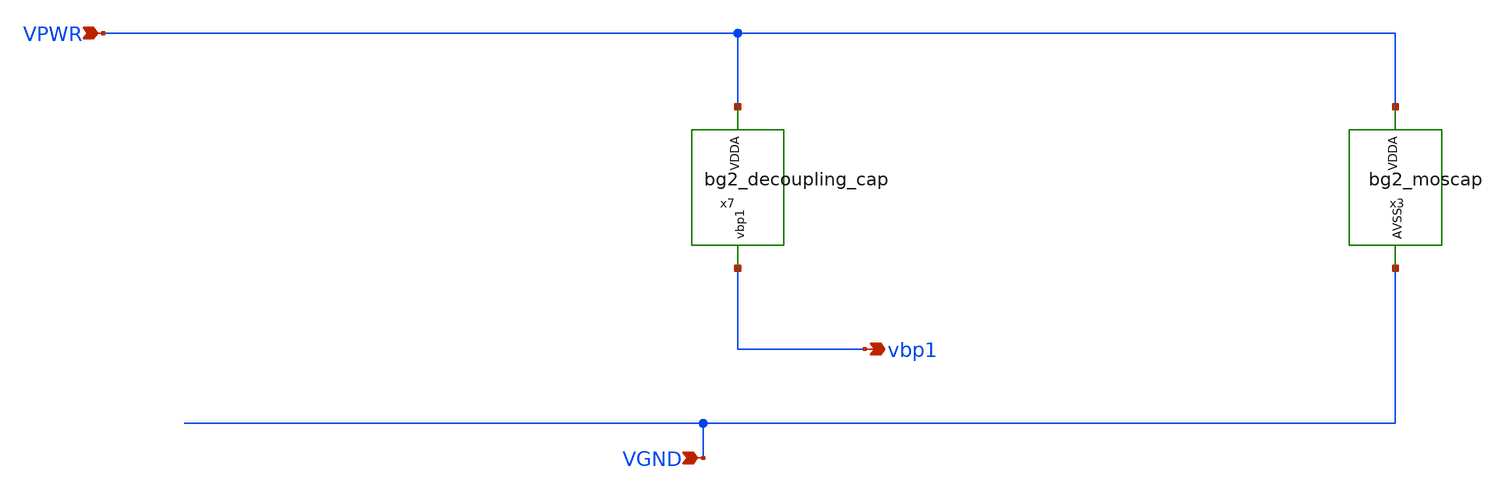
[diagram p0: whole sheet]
** sch_path: lef/lef/gds/bg2_top_tt_v2.sch
**.subckt bg2_top_tt_v2 VGND VPWR vbp1
*.ipin VGND
*.ipin VPWR
*.opin vbp1
x3 VPWR VGND bg2_moscap
x7 VPWR vbp1 bg2_decoupling_cap
**.ends
.end
